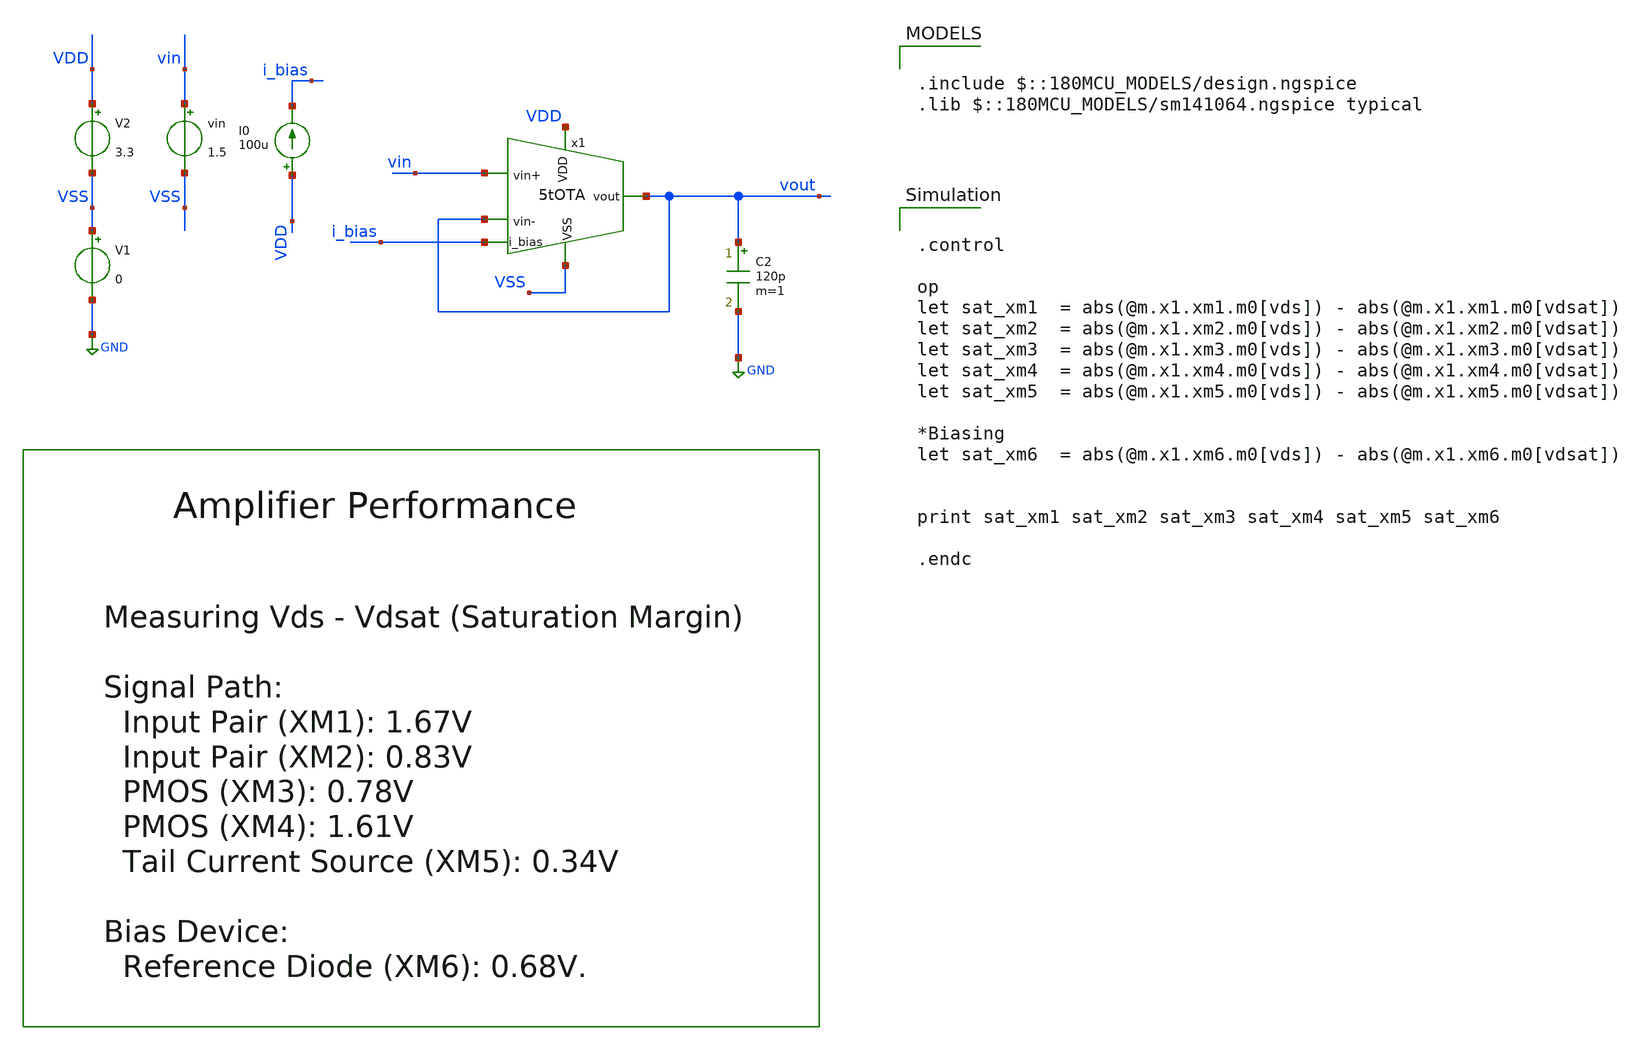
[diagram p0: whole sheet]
** sch_path: designs/libs/core_amps/ota_5t/tb/5tOTA_tb_op_vds.sch
**.subckt 5tOTA_tb_op_vds
V1 VSS GND 0
V2 VDD VSS 3.3
I0 VDD i_bias 100u
vin vin VSS 1.5
C2 vout GND 120p m=1
x1 VDD vout vin vout i_bias VSS 5tOTA
**** begin user architecture code

.include $::180MCU_MODELS/design.ngspice
.lib $::180MCU_MODELS/sm141064.ngspice typical



.control

op
let sat_xm1  = abs(@m.x1.xm1.m0[vds]) - abs(@m.x1.xm1.m0[vdsat])
let sat_xm2  = abs(@m.x1.xm2.m0[vds]) - abs(@m.x1.xm2.m0[vdsat])
let sat_xm3  = abs(@m.x1.xm3.m0[vds]) - abs(@m.x1.xm3.m0[vdsat])
let sat_xm4  = abs(@m.x1.xm4.m0[vds]) - abs(@m.x1.xm4.m0[vdsat])
let sat_xm5  = abs(@m.x1.xm5.m0[vds]) - abs(@m.x1.xm5.m0[vdsat])

*Biasing
let sat_xm6  = abs(@m.x1.xm6.m0[vds]) - abs(@m.x1.xm6.m0[vdsat])


print sat_xm1 sat_xm2 sat_xm3 sat_xm4 sat_xm5 sat_xm6

.endc


**** end user architecture code
**.ends

* expanding   symbol:  libs/core_amps/ota_5t/schem/5tOTA.sym # of pins=6
** sym_path: designs/5tOTA.sym
** sch_path: designs/5tOTA.sch
.subckt 5tOTA VDD vout vin+ vin- i_bias VSS
*.ipin VDD
*.opin vout
*.ipin i_bias
*.ipin vin+
*.ipin vin-
*.ipin VSS
XM1 net1 vin+ net2 VSS nfet_03v3 L=0.5u W=11.43u nf=1 ad='int((nf+1)/2) * W/nf * 0.18u' as='int((nf+2)/2) * W/nf * 0.18u'
+ pd='2*int((nf+1)/2) * (W/nf + 0.18u)' ps='2*int((nf+2)/2) * (W/nf + 0.18u)' nrd='0.18u / W' nrs='0.18u / W'
+ sa=0 sb=0 sd=0 m=1
XM2 vout vin- net2 VSS nfet_03v3 L=0.5u W=11.43u nf=1 ad='int((nf+1)/2) * W/nf * 0.18u' as='int((nf+2)/2) * W/nf * 0.18u'
+ pd='2*int((nf+1)/2) * (W/nf + 0.18u)' ps='2*int((nf+2)/2) * (W/nf + 0.18u)' nrd='0.18u / W' nrs='0.18u / W'
+ sa=0 sb=0 sd=0 m=1
XM3 net1 net1 VDD VDD pfet_03v3 L=0.5u W=22.86u nf=1 ad='int((nf+1)/2) * W/nf * 0.18u' as='int((nf+2)/2) * W/nf * 0.18u'
+ pd='2*int((nf+1)/2) * (W/nf + 0.18u)' ps='2*int((nf+2)/2) * (W/nf + 0.18u)' nrd='0.18u / W' nrs='0.18u / W'
+ sa=0 sb=0 sd=0 m=1
XM4 vout net1 VDD VDD pfet_03v3 L=0.5u W=22.86u nf=1 ad='int((nf+1)/2) * W/nf * 0.18u' as='int((nf+2)/2) * W/nf * 0.18u'
+ pd='2*int((nf+1)/2) * (W/nf + 0.18u)' ps='2*int((nf+2)/2) * (W/nf + 0.18u)' nrd='0.18u / W' nrs='0.18u / W'
+ sa=0 sb=0 sd=0 m=1
XM5 net2 i_bias VSS VSS nfet_03v3 L=0.5u W=22.86u nf=1 ad='int((nf+1)/2) * W/nf * 0.18u' as='int((nf+2)/2) * W/nf * 0.18u'
+ pd='2*int((nf+1)/2) * (W/nf + 0.18u)' ps='2*int((nf+2)/2) * (W/nf + 0.18u)' nrd='0.18u / W' nrs='0.18u / W'
+ sa=0 sb=0 sd=0 m=1
XM6 i_bias i_bias VSS VSS nfet_03v3 L=0.5u W=22.86u nf=1 ad='int((nf+1)/2) * W/nf * 0.18u' as='int((nf+2)/2) * W/nf * 0.18u'
+ pd='2*int((nf+1)/2) * (W/nf + 0.18u)' ps='2*int((nf+2)/2) * (W/nf + 0.18u)' nrd='0.18u / W' nrs='0.18u / W'
+ sa=0 sb=0 sd=0 m=1
.ends

.GLOBAL GND
.end
